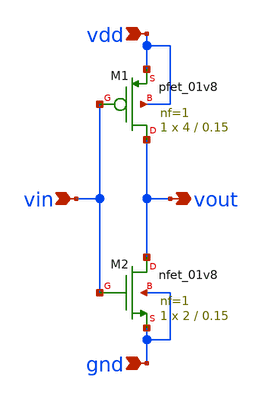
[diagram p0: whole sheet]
** sch_path: Xschem-Files/invt_vtc.sch
**.subckt invt_vtc vin vdd gnd vout
*.ipin vin
*.ipin vdd
*.ipin gnd
*.opin vout
XM1 vout vin vdd vdd sky130_fd_pr__pfet_01v8 L=0.15 W=4 nf=1 ad='int((1 + 1)/2) * 4 / 1 * 0.29' as='int((1 + 2)/2) * 4 / 1 * 0.29'
+ pd='2*int((1 + 1)/2) * (4 / 1 + 0.29)' ps='2*int((1 + 2)/2) * (4 / 1 + 0.29)' nrd='0.29 / 4 ' nrs='0.29 / 4 '
+ sa=0 sb=0 sd=0 mult=1 m=1
XM2 vout vin gnd gnd sky130_fd_pr__nfet_01v8 L=0.15 W=2 nf=1 ad='int((1 + 1)/2) * 2 / 1 * 0.29' as='int((1 + 2)/2) * 2 / 1 * 0.29'
+ pd='2*int((1 + 1)/2) * (2 / 1 + 0.29)' ps='2*int((1 + 2)/2) * (2 / 1 + 0.29)' nrd='0.29 / 2 ' nrs='0.29 / 2 '
+ sa=0 sb=0 sd=0 mult=1 m=1
**.ends
.end
